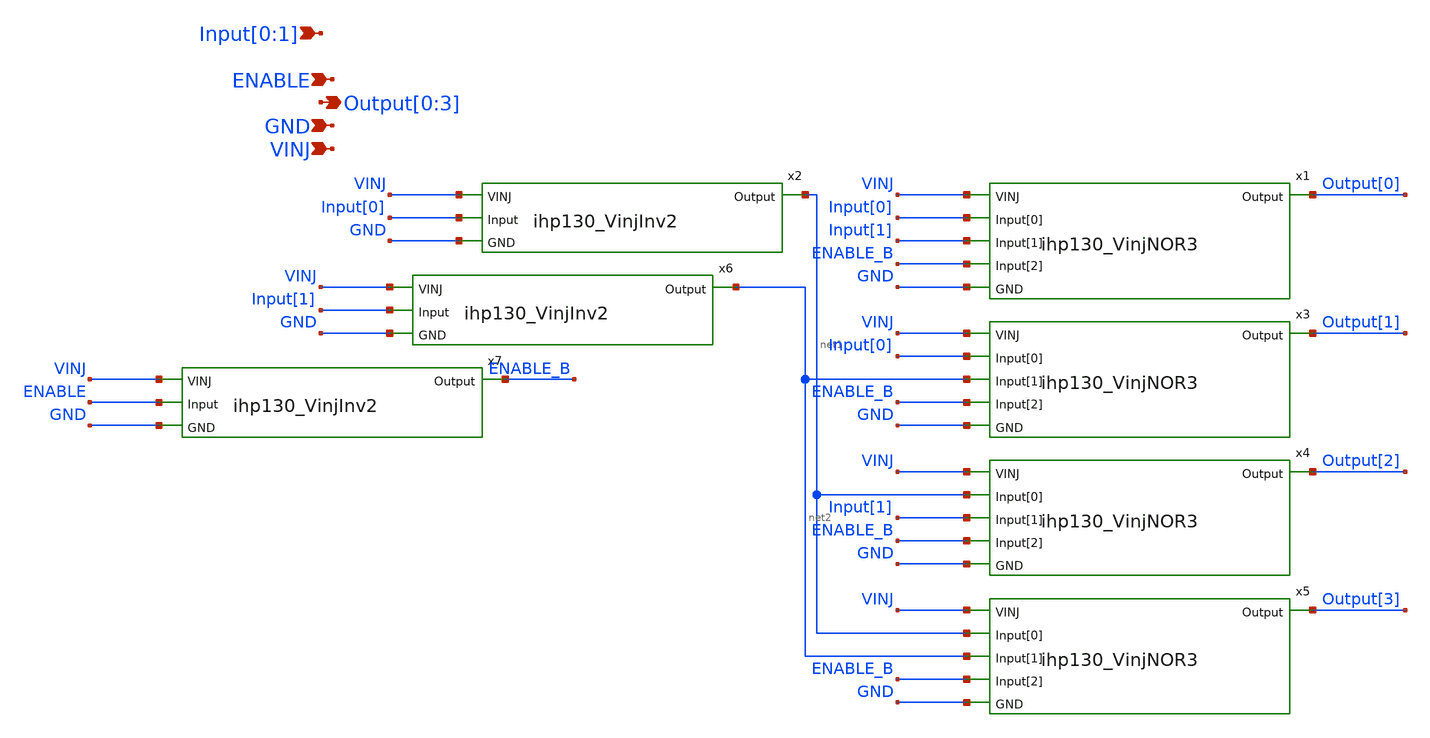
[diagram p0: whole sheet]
** sch_path: ihp130_cells/VinjDec2_to_4/ihp130_VinjDec2_to_4.sch
**.subckt ihp130_VinjDec2_to_4 VINJ Output[0],Output[1],Output[2],Output[3] Input[0],Input[1] GND
*+ ENABLE
*.ipin VINJ
*.opin Output[0],Output[1],Output[2],Output[3]
*.ipin Input[0],Input[1]
*.ipin GND
*.ipin ENABLE
x2 VINJ Input[0] net1 GND ihp130_VinjInv2
x6 VINJ Input[1] net2 GND ihp130_VinjInv2
x7 VINJ ENABLE ENABLE_B GND ihp130_VinjInv2
x1 VINJ Input[0] Input[1] Output[0] ENABLE_B GND ihp130_VinjNOR3
x3 VINJ Input[0] net2 Output[1] ENABLE_B GND ihp130_VinjNOR3
x4 VINJ net1 Input[1] Output[2] ENABLE_B GND ihp130_VinjNOR3
x5 VINJ net1 net2 Output[3] ENABLE_B GND ihp130_VinjNOR3
**.ends

* expanding   symbol:  VinjInv2/ihp130_VinjInv2.sym # of pins=4
** sym_path: ihp130_cells/VinjInv2/ihp130_VinjInv2.sym
** sch_path: ihp130_cells/VinjInv2/ihp130_VinjInv2.sch
.subckt ihp130_VinjInv2 VINJ Input Output GND
*.ipin VINJ
*.ipin GND
*.ipin Input
*.opin Output
XM1 Output Input GND GND sg13_hv_nmos w=0.42u l=0.53u ng=1 m=1 mm_ok=1
XM2 Output Input VINJ VINJ sg13_hv_pmos w=0.42u l=0.53u ng=1 m=1 mm_ok=1
.ends


* expanding   symbol:  VinjNOR3/ihp130_VinjNOR3.sym # of pins=6
** sym_path: ihp130_cells/VinjNOR3/ihp130_VinjNOR3.sym
** sch_path: ihp130_cells/VinjNOR3/ihp130_VinjNOR3.sch
.subckt ihp130_VinjNOR3 VINJ Input[0] Input[1] Output Input[2] GND
*.ipin Input[0]
*.ipin VINJ
*.ipin GND
*.opin Output
*.ipin Input[1]
*.ipin Input[2]
XM1 net1 Input[2] VINJ VINJ sg13_hv_pmos w=0.42u l=0.53u ng=1 m=1 mm_ok=1
XM2 net2 Input[0] net1 VINJ sg13_hv_pmos w=0.42u l=0.53u ng=1 m=1 mm_ok=1
XM3 Output Input[1] net2 VINJ sg13_hv_pmos w=0.42u l=0.53u ng=1 m=1 mm_ok=1
XM4 Output Input[1] GND GND sg13_hv_nmos w=0.42u l=0.5u ng=1 m=1 mm_ok=1
XM5 Output Input[2] GND GND sg13_hv_nmos w=0.42u l=0.5u ng=1 m=1 mm_ok=1
XM6 Output Input[0] GND GND sg13_hv_nmos w=0.42u l=0.5u ng=1 m=1 mm_ok=1
.ends

.end
